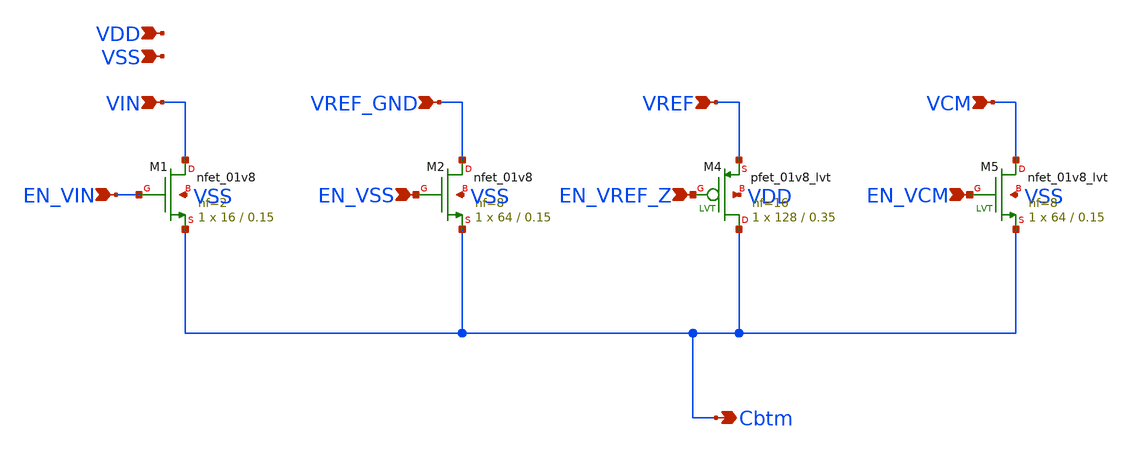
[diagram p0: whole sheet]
** sch_path: individual_switches/switch_C10.sch
**.subckt switch_C10 VIN EN_VIN VREF_GND VREF VCM EN_VCM Cbtm VDD EN_VSS EN_VREF_Z VSS
*.ipin VIN
*.ipin EN_VIN
*.ipin VREF_GND
*.ipin VREF
*.ipin VCM
*.ipin EN_VCM
*.opin Cbtm
*.ipin VDD
*.ipin EN_VSS
*.ipin EN_VREF_Z
*.ipin VSS
XM1 VIN EN_VIN Cbtm VSS sky130_fd_pr__nfet_01v8 L=0.15 W=16 nf=2 ad='int((nf+1)/2) * W/nf * 0.29' as='int((nf+2)/2) * W/nf * 0.29'
+ pd='2*int((nf+1)/2) * (W/nf + 0.29)' ps='2*int((nf+2)/2) * (W/nf + 0.29)' nrd='0.29 / W' nrs='0.29 / W'
+ sa=0 sb=0 sd=0 mult=1 m=1
XM2 VREF_GND EN_VSS Cbtm VSS sky130_fd_pr__nfet_01v8 L=0.15 W=64 nf=8 ad='int((nf+1)/2) * W/nf * 0.29'
+ as='int((nf+2)/2) * W/nf * 0.29' pd='2*int((nf+1)/2) * (W/nf + 0.29)' ps='2*int((nf+2)/2) * (W/nf + 0.29)'
+ nrd='0.29 / W' nrs='0.29 / W' sa=0 sb=0 sd=0 mult=1 m=1
XM4 Cbtm EN_VREF_Z VREF VDD sky130_fd_pr__pfet_01v8_lvt L=0.35 W=128 nf=16 ad='int((nf+1)/2) * W/nf * 0.29'
+ as='int((nf+2)/2) * W/nf * 0.29' pd='2*int((nf+1)/2) * (W/nf + 0.29)' ps='2*int((nf+2)/2) * (W/nf + 0.29)'
+ nrd='0.29 / W' nrs='0.29 / W' sa=0 sb=0 sd=0 mult=1 m=1
XM5 VCM EN_VCM Cbtm VSS sky130_fd_pr__nfet_01v8_lvt L=0.15 W=64 nf=8 ad='int((nf+1)/2) * W/nf * 0.29'
+ as='int((nf+2)/2) * W/nf * 0.29' pd='2*int((nf+1)/2) * (W/nf + 0.29)' ps='2*int((nf+2)/2) * (W/nf + 0.29)'
+ nrd='0.29 / W' nrs='0.29 / W' sa=0 sb=0 sd=0 mult=1 m=1
**.ends
.end
